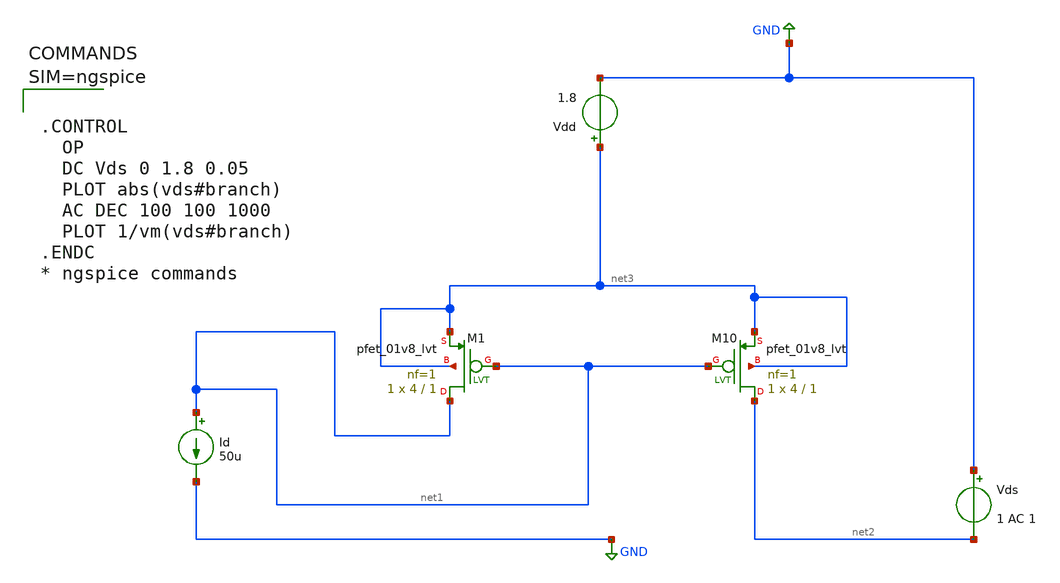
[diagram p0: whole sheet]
** sch_path: xschem/currmirrorpmos.sch
**.subckt currmirrorpmos
XM10 net2 net1 net3 net3 sky130_fd_pr__pfet_01v8_lvt L=1 W=4 nf=1 ad='int((1 + 1)/2) * 4 / 1 * 0.29'
+ as='int((1 + 2)/2) * 4 / 1 * 0.29' pd='2*int((1 + 1)/2) * (4 / 1 + 0.29)' ps='2*int((1 + 2)/2) * (4 / 1 + 0.29)'
+ nrd='0.29 / 4 ' nrs='0.29 / 4 ' sa=0 sb=0 sd=0 mult=1 m=1
XM1 net1 net1 net3 net3 sky130_fd_pr__pfet_01v8_lvt L=1 W=4 nf=1 ad='int((1 + 1)/2) * 4 / 1 * 0.29' as='int((1 + 2)/2) * 4 / 1 * 0.29'
+ pd='2*int((1 + 1)/2) * (4 / 1 + 0.29)' ps='2*int((1 + 2)/2) * (4 / 1 + 0.29)' nrd='0.29 / 4 ' nrs='0.29 / 4 '
+ sa=0 sb=0 sd=0 mult=1 m=1
Id net1 GND 50u
Vds GND net2 1 AC 1
Vdd net3 GND 1.8
**** begin user architecture code

** opencircuitdesign pdks install
.lib $::SKYWATER_MODELS/sky130.lib.spice tt




.CONTROL
  OP
  DC Vds 0 1.8 0.05
  PLOT abs(vds#branch)
  AC DEC 100 100 1000
  PLOT 1/vm(vds#branch)
.ENDC
* ngspice commands



**** end user architecture code
**.ends
.GLOBAL GND
.end
